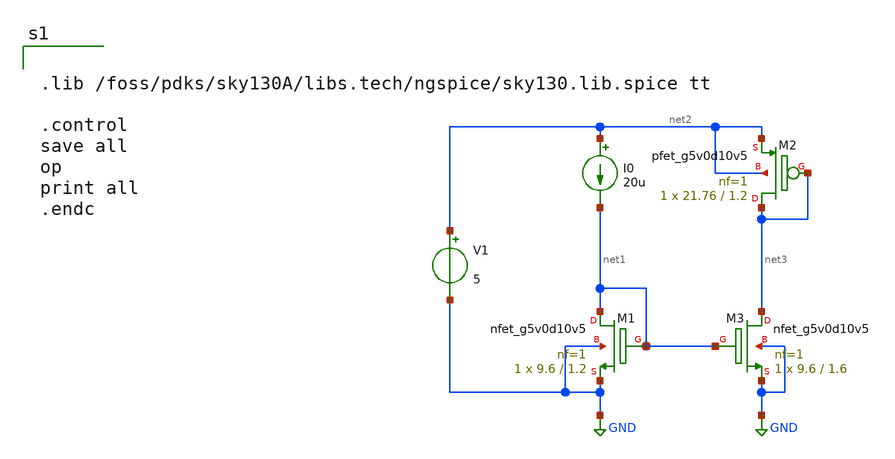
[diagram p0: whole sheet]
** sch_path: simple_mirror.sch
**.subckt simple_mirror
XM1 net1 net1 GND GND sky130_fd_pr__nfet_g5v0d10v5 L=1.2 W=9.6 nf=1 ad='int((nf+1)/2) * W/nf * 0.29'
+ as='int((nf+2)/2) * W/nf * 0.29' pd='2*int((nf+1)/2) * (W/nf + 0.29)' ps='2*int((nf+2)/2) * (W/nf + 0.29)'
+ nrd='0.29 / W' nrs='0.29 / W' sa=0 sb=0 sd=0 mult=1 m=1
XM2 net3 net3 net2 net2 sky130_fd_pr__pfet_g5v0d10v5 L=1.2 W=21.76 nf=1 ad='int((nf+1)/2) * W/nf * 0.29'
+ as='int((nf+2)/2) * W/nf * 0.29' pd='2*int((nf+1)/2) * (W/nf + 0.29)' ps='2*int((nf+2)/2) * (W/nf + 0.29)'
+ nrd='0.29 / W' nrs='0.29 / W' sa=0 sb=0 sd=0 mult=1 m=1
I0 net2 net1 20u
V1 net2 GND 5
XM3 net3 net1 GND GND sky130_fd_pr__nfet_g5v0d10v5 L=1.6 W=9.6 nf=1 ad='int((nf+1)/2) * W/nf * 0.29'
+ as='int((nf+2)/2) * W/nf * 0.29' pd='2*int((nf+1)/2) * (W/nf + 0.29)' ps='2*int((nf+2)/2) * (W/nf + 0.29)'
+ nrd='0.29 / W' nrs='0.29 / W' sa=0 sb=0 sd=0 mult=1 m=1
**** begin user architecture code


.lib /foss/pdks/sky130A/libs.tech/ngspice/sky130.lib.spice tt

.control
save all
op
print all
.endc


**** end user architecture code
**.ends
.GLOBAL GND
.end
